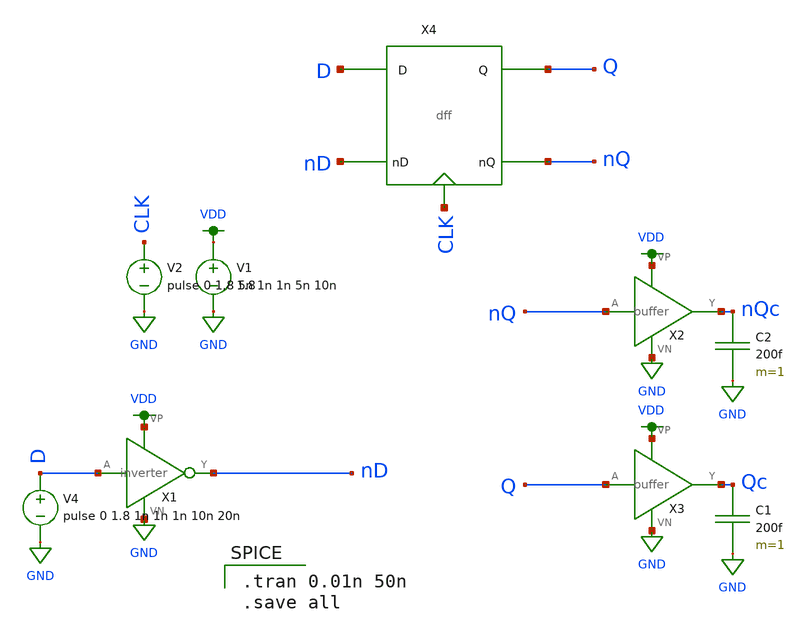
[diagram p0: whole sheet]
** sch_path: mini2/schem/dff_test.sch
**.subckt dff_test
V1 VDD GND 1.8
V2 CLK GND pulse 0 1.8 5n 1n 1n 5n 10n
V4 D GND pulse 0 1.8 1n 1n 1n 10n 20n
X1 D nD VDD GND inverter
C1 Qc GND 200f m=1
C2 nQc GND 200f m=1
X2 nQ nQc VDD GND buffer
X3 Q Qc VDD GND buffer
X4 D nD CLK nQ Q dff
**** begin user architecture code

.option wnflag=1
.lib ~/skywater/skywater-pdk/libraries/sky130_fd_pr_ngspice/latest/models/sky130.lib.spice tt


.tran 0.01n 50n
.save all

**** end user architecture code
**.ends
.GLOBAL VDD
.GLOBAL GND
.end
